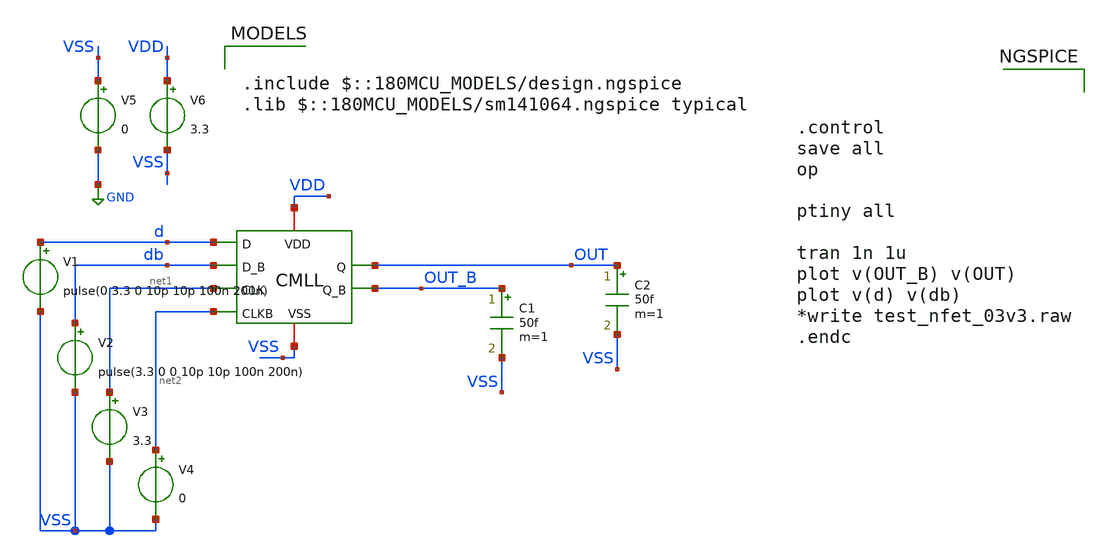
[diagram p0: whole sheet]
** sch_path: DAC_PAKISTAN_01/Pakistan1_Xschem/CMLL_TB.sch
**.subckt CMLL_TB
x1 VDD VSS d db net1 net2 OUT OUT_B CMLL
V1 d VSS pulse(0 3.3 0 10p 10p 100n 200n)
V2 db VSS pulse(3.3 0 0 10p 10p 100n 200n)
V3 net1 VSS 3.3
V4 net2 VSS 0
V5 VSS GND 0
V6 VDD VSS 3.3
C1 OUT_B VSS 50f m=1
C2 OUT VSS 50f m=1
**** begin user architecture code

.include $::180MCU_MODELS/design.ngspice
.lib $::180MCU_MODELS/sm141064.ngspice typical




.control
save all
op

ptiny all

tran 1n 1u
plot v(OUT_B) v(OUT)
plot v(d) v(db)
*write test_nfet_03v3.raw
.endc


**** end user architecture code
**.ends

* expanding   symbol:  CMLL.sym # of pins=8
** sym_path: DAC_PAKISTAN_01/Pakistan1_Xschem/CMLL.sym
** sch_path: DAC_PAKISTAN_01/Pakistan1_Xschem/CMLL.sch
.subckt CMLL VDD VSS D D_B CLK CLKB Q Q_B
*.iopin VDD
*.iopin VSS
*.ipin D
*.ipin D_B
*.ipin CLK
*.ipin CLKB
*.opin Q
*.opin Q_B
XM2 Q D_B net1 VSS nfet_03v3 L=0.28u W=1u nf=1 ad='int((nf+1)/2) * W/nf * 0.18u' as='int((nf+2)/2) * W/nf * 0.18u'
+ pd='2*int((nf+1)/2) * (W/nf + 0.18u)' ps='2*int((nf+2)/2) * (W/nf + 0.18u)' nrd='0.18u / W' nrs='0.18u / W'
+ sa=0 sb=0 sd=0 m=1
XM3 Q Q_B net2 VSS nfet_03v3 L=0.28u W=0.22u nf=1 ad='int((nf+1)/2) * W/nf * 0.18u' as='int((nf+2)/2) * W/nf * 0.18u'
+ pd='2*int((nf+1)/2) * (W/nf + 0.18u)' ps='2*int((nf+2)/2) * (W/nf + 0.18u)' nrd='0.18u / W' nrs='0.18u / W'
+ sa=0 sb=0 sd=0 m=1
XM4 Q_B Q net2 VSS nfet_03v3 L=0.28u W=0.22u nf=1 ad='int((nf+1)/2) * W/nf * 0.18u' as='int((nf+2)/2) * W/nf * 0.18u'
+ pd='2*int((nf+1)/2) * (W/nf + 0.18u)' ps='2*int((nf+2)/2) * (W/nf + 0.18u)' nrd='0.18u / W' nrs='0.18u / W'
+ sa=0 sb=0 sd=0 m=1
XM5 net2 CLKB net3 VSS nfet_03v3 L=0.28u W=0.22u nf=1 ad='int((nf+1)/2) * W/nf * 0.18u' as='int((nf+2)/2) * W/nf * 0.18u'
+ pd='2*int((nf+1)/2) * (W/nf + 0.18u)' ps='2*int((nf+2)/2) * (W/nf + 0.18u)' nrd='0.18u / W' nrs='0.18u / W'
+ sa=0 sb=0 sd=0 m=1
XM6 Q_B D net1 VSS nfet_03v3 L=0.28u W=1u nf=1 ad='int((nf+1)/2) * W/nf * 0.18u' as='int((nf+2)/2) * W/nf * 0.18u'
+ pd='2*int((nf+1)/2) * (W/nf + 0.18u)' ps='2*int((nf+2)/2) * (W/nf + 0.18u)' nrd='0.18u / W' nrs='0.18u / W'
+ sa=0 sb=0 sd=0 m=1
R1 VDD Q_B 20k m=1
R2 VDD Q 20k m=1
I0 net3 VSS 50u
XM1 net1 CLK net3 VSS nfet_03v3 L=0.28u W=1u nf=1 ad='int((nf+1)/2) * W/nf * 0.18u' as='int((nf+2)/2) * W/nf * 0.18u'
+ pd='2*int((nf+1)/2) * (W/nf + 0.18u)' ps='2*int((nf+2)/2) * (W/nf + 0.18u)' nrd='0.18u / W' nrs='0.18u / W'
+ sa=0 sb=0 sd=0 m=1
.ends

.GLOBAL GND
.end
